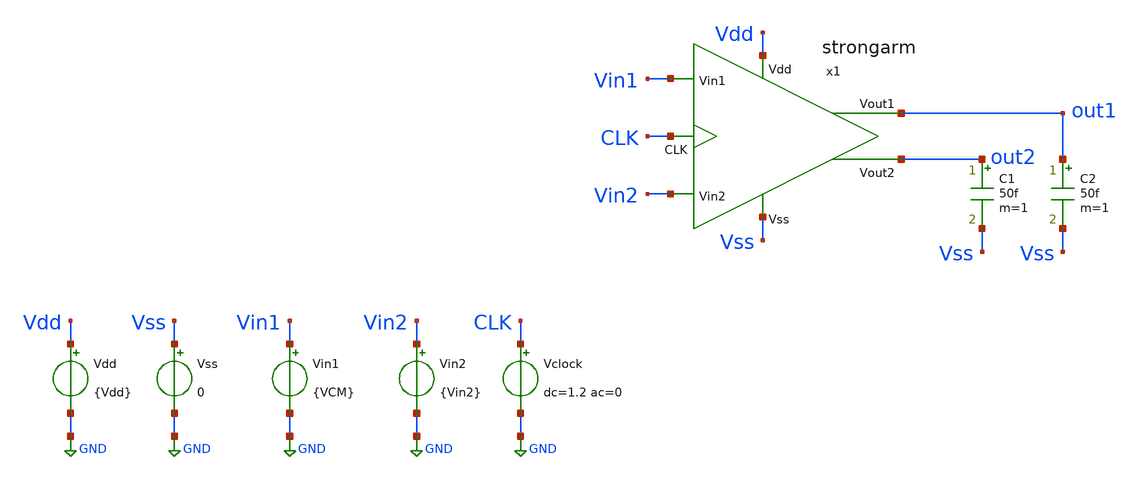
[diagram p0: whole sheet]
** sch_path: xschem/TB/TB_Op_SA.sch
**.subckt TB_Op_SA
Vdd Vdd GND {Vdd}
x1 out2 out1 Vdd Vss Vin2 Vin1 CLK strongarm
Vss Vss GND 0
C1 out2 Vss 50f m=1
C2 out1 Vss 50f m=1
Vin1 Vin1 GND {VCM}
Vin2 Vin2 GND {Vin2}
Vclock CLK GND dc=1.2 ac=0
**** begin user architecture code


.param Vdd = 1.2
.param ACM = 10m
.param FCM = 10MEG
.param VCM = 0.6
.param Vin2 = VCM

* parametros de sweep para offset
.param V_strt = 0.4
.param V_stop = 0.8
.param V_step = 1m
.param V_curr = 0.4

.ic v(x1.P) = 1.2
.ic v(x1.Q) = 1.2
.ic v(out1) = 1.2
.ic v(out2) = 1.2





.lib cornerMOSlv.lib mos_tt




** TRANSISTORES NMOS

.param W12 = 1.0u
.param L12 = 0.13u
.param M12 = 1

.param W34 = 1.0u
.param L34 = 0.13u
.param M34 = 1

.param W56 = 1.0u
.param L56 = 0.13u
.param M56 = 1

.param W7  = 1.0u
.param L7  = 0.13u
.param M7  = 1

.param W89 = 1.0u
.param L89 = 0.13u
.param M89 = 1

.param Wab = 1.0u
.param Lab = 0.13u
.param Mab = 1




.control
save all  @n.x1.xm1.nsg13_lv_nmos[gm]  @n.x1.xm2.nsg13_lv_nmos[gm]  @n.x1.xm1.nsg13_lv_nmos[ids]
+  @n.x1.xm2.nsg13_lv_nmos[ids]

while V_curr le V_stop
    alterparam Vin2 = $&V_curr
    reset
    save all
    op
    wrdata ao_sweep_l.raw ao
    set appendwrite

    let V_curr = V_curr + V_step
end
.endc


**** end user architecture code
**.ends

* expanding   symbol:  ../sch/strongarm.sym # of pins=7
** sym_path: xschem/sch/strongarm.sym
** sch_path: xschem/sch/strongarm.sch
.subckt strongarm Vout2 Vout1 Vdd Vss Vin2 Vin1 CLK
*.opin Vout2
*.opin Vout1
*.ipin Vin1
*.ipin Vin2
*.ipin CLK
*.ipin Vss
*.ipin Vdd
XM1 common Vin1 P Vss sg13_lv_nmos w={W12} l={L12} ng=1 m={M12} mm_ok=1
XM2 common Vin2 Q Vss sg13_lv_nmos w={W12} l={L12} ng=1 m={M12} mm_ok=1
XM3 P Voq Vop Vss sg13_lv_nmos w={W34} l={L34} ng=1 m={M34} mm_ok=1
XM4 Q Vop Voq Vss sg13_lv_nmos w={W34} l={L34} ng=1 m={M34} mm_ok=1
XM6 Voq Vop Vdd Vdd sg13_lv_pmos w={W56} l={L56} ng=1 m={M56} mm_ok=1
XM5 Vop Voq Vdd Vdd sg13_lv_pmos w={W56} l={L56} ng=1 m={M56} mm_ok=1
XM7 Vss CLK common Vss sg13_lv_nmos w={W7} l={L7} ng=1 m={M7} mm_ok=1
XM8 P CLK Vdd Vdd sg13_lv_pmos w={W89} l={L89} ng=1 m={M89} mm_ok=1
XM9 Q CLK Vdd Vdd sg13_lv_pmos w={W89} l={L89} ng=1 m={M89} mm_ok=1
XM11 Voq CLK Vdd Vdd sg13_lv_pmos w={Wab} l={Lab} ng=1 m={Wab} mm_ok=1
XM10 Vop CLK Vdd Vdd sg13_lv_pmos w={Wab} l={Lab} ng=1 m={Wab} mm_ok=1
.ends

.GLOBAL GND
.end
